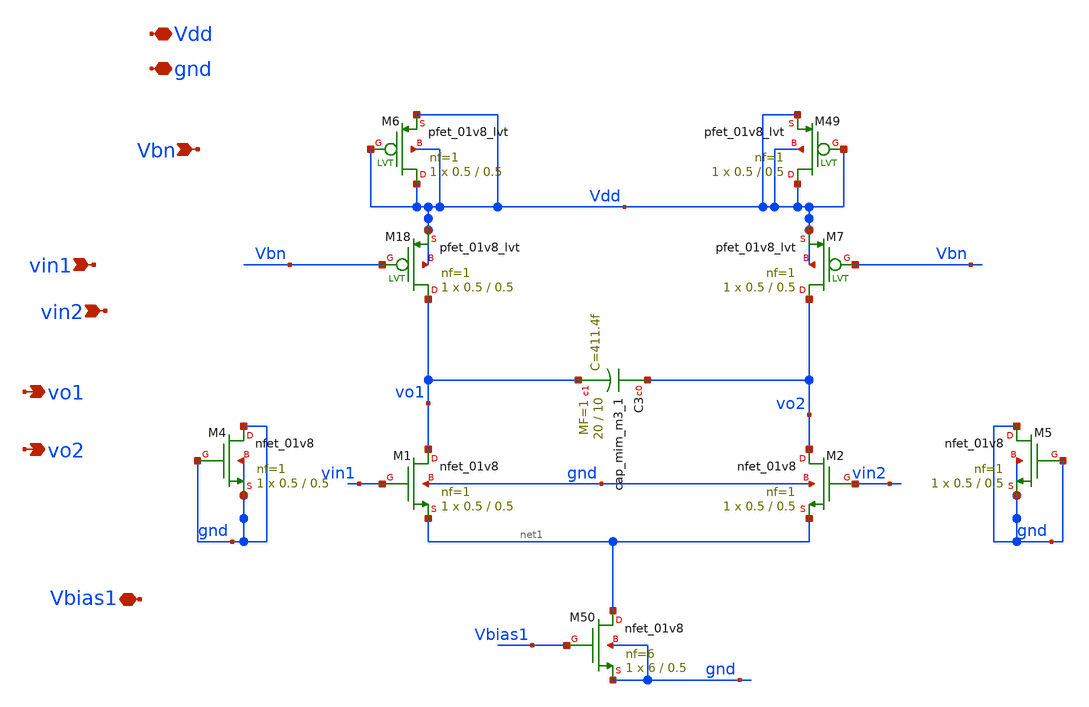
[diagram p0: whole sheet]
** sch_path: xschem/charge_pumps2/integrator_lvs.sch
**.subckt integrator_lvs gnd Vdd Vbn vin1 vin2 vo1 vo2 Vbias1
*.iopin gnd
*.iopin Vdd
*.ipin Vbn
*.ipin vin1
*.ipin vin2
*.opin vo1
*.opin vo2
*.iopin Vbias1
XM1 vo1 vin1 net1 gnd sky130_fd_pr__nfet_01v8 L=0.5 W=0.5 nf=1 ad='int((nf+1)/2) * W/nf * 0.29' as='int((nf+2)/2) * W/nf * 0.29'
+ pd='2*int((nf+1)/2) * (W/nf + 0.29)' ps='2*int((nf+2)/2) * (W/nf + 0.29)' nrd='0.29 / W' nrs='0.29 / W'
+ sa=0 sb=0 sd=0 mult=1 m=1
XM2 vo2 vin2 net1 gnd sky130_fd_pr__nfet_01v8 L=0.5 W=0.5 nf=1 ad='int((nf+1)/2) * W/nf * 0.29' as='int((nf+2)/2) * W/nf * 0.29'
+ pd='2*int((nf+1)/2) * (W/nf + 0.29)' ps='2*int((nf+2)/2) * (W/nf + 0.29)' nrd='0.29 / W' nrs='0.29 / W'
+ sa=0 sb=0 sd=0 mult=1 m=1
XC3 vo2 vo1 sky130_fd_pr__cap_mim_m3_1 W=20 L=10 MF=1 m=1
XM4 gnd gnd gnd gnd sky130_fd_pr__nfet_01v8 L=0.5 W=0.5 nf=1 ad='int((nf+1)/2) * W/nf * 0.29' as='int((nf+2)/2) * W/nf * 0.29'
+ pd='2*int((nf+1)/2) * (W/nf + 0.29)' ps='2*int((nf+2)/2) * (W/nf + 0.29)' nrd='0.29 / W' nrs='0.29 / W'
+ sa=0 sb=0 sd=0 mult=1 m=1
XM5 gnd gnd gnd gnd sky130_fd_pr__nfet_01v8 L=0.5 W=0.5 nf=1 ad='int((nf+1)/2) * W/nf * 0.29' as='int((nf+2)/2) * W/nf * 0.29'
+ pd='2*int((nf+1)/2) * (W/nf + 0.29)' ps='2*int((nf+2)/2) * (W/nf + 0.29)' nrd='0.29 / W' nrs='0.29 / W'
+ sa=0 sb=0 sd=0 mult=1 m=1
XM18 vo1 Vbn Vdd Vdd sky130_fd_pr__pfet_01v8_lvt L=0.5 W=0.5 nf=1 ad='int((nf+1)/2) * W/nf * 0.29' as='int((nf+2)/2) * W/nf * 0.29'
+ pd='2*int((nf+1)/2) * (W/nf + 0.29)' ps='2*int((nf+2)/2) * (W/nf + 0.29)' nrd='0.29 / W' nrs='0.29 / W'
+ sa=0 sb=0 sd=0 mult=1 m=1
XM6 Vdd Vdd Vdd Vdd sky130_fd_pr__pfet_01v8_lvt L=0.5 W=0.5 nf=1 ad='int((nf+1)/2) * W/nf * 0.29' as='int((nf+2)/2) * W/nf * 0.29'
+ pd='2*int((nf+1)/2) * (W/nf + 0.29)' ps='2*int((nf+2)/2) * (W/nf + 0.29)' nrd='0.29 / W' nrs='0.29 / W'
+ sa=0 sb=0 sd=0 mult=1 m=1
XM7 vo2 Vbn Vdd Vdd sky130_fd_pr__pfet_01v8_lvt L=0.5 W=0.5 nf=1 ad='int((nf+1)/2) * W/nf * 0.29' as='int((nf+2)/2) * W/nf * 0.29'
+ pd='2*int((nf+1)/2) * (W/nf + 0.29)' ps='2*int((nf+2)/2) * (W/nf + 0.29)' nrd='0.29 / W' nrs='0.29 / W'
+ sa=0 sb=0 sd=0 mult=1 m=1
XM49 Vdd Vdd Vdd Vdd sky130_fd_pr__pfet_01v8_lvt L=0.5 W=0.5 nf=1 ad='int((nf+1)/2) * W/nf * 0.29' as='int((nf+2)/2) * W/nf * 0.29'
+ pd='2*int((nf+1)/2) * (W/nf + 0.29)' ps='2*int((nf+2)/2) * (W/nf + 0.29)' nrd='0.29 / W' nrs='0.29 / W'
+ sa=0 sb=0 sd=0 mult=1 m=1
XM50 net1 Vbias1 gnd gnd sky130_fd_pr__nfet_01v8 L=0.5 W=6 nf=6 ad='int((nf+1)/2) * W/nf * 0.29' as='int((nf+2)/2) * W/nf * 0.29'
+ pd='2*int((nf+1)/2) * (W/nf + 0.29)' ps='2*int((nf+2)/2) * (W/nf + 0.29)' nrd='0.29 / W' nrs='0.29 / W'
+ sa=0 sb=0 sd=0 mult=1 m=1
**.ends
.end
